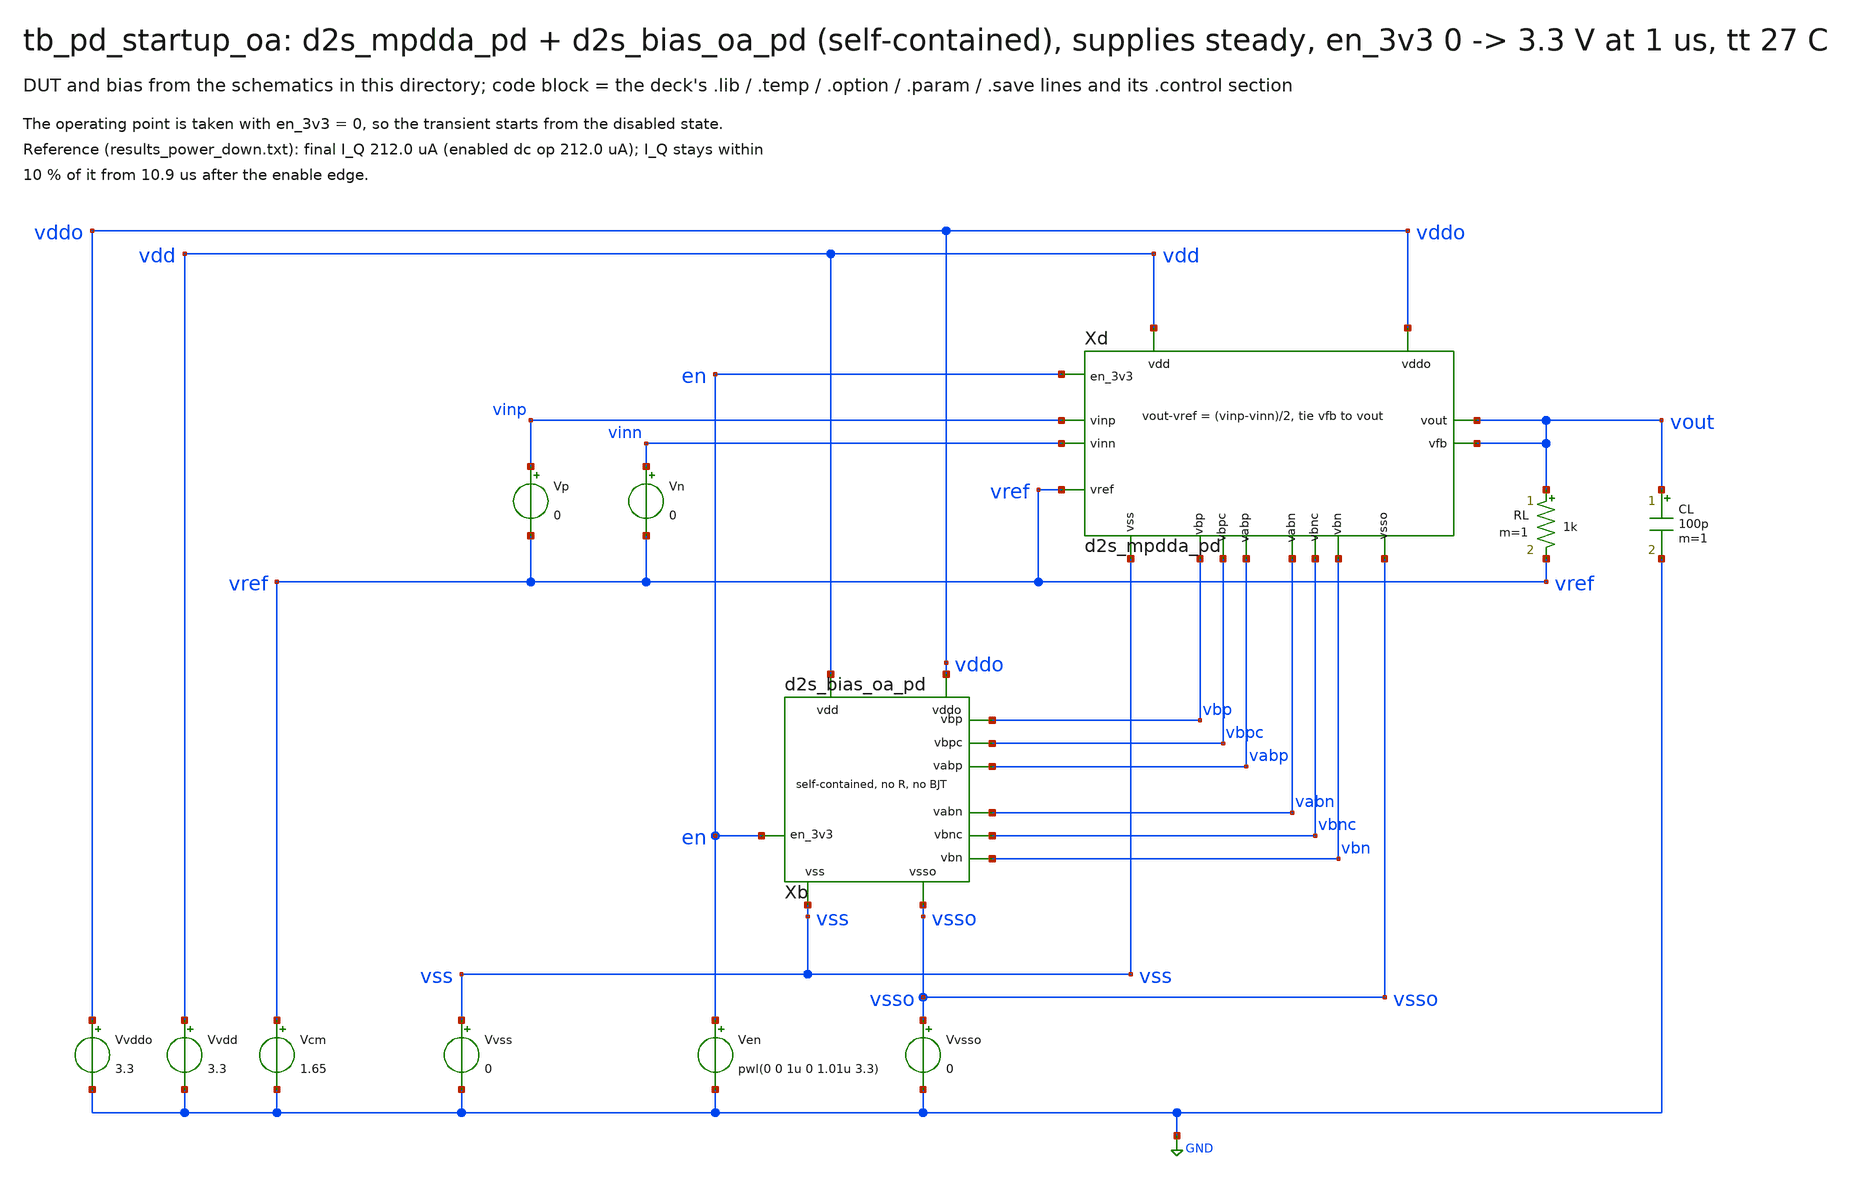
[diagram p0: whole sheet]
** sch_path: sudelbuecher/design_considerations/consolidation/enable_rework_2026-10-25/before/macros/sg13cmos5l_IOPadDiff2Single/testbenches/xschem/tb_pd_startup_oa.sch
**.subckt tb_pd_startup_oa
Vvdd vdd GND 3.3
Vvss vss GND 0
Vvddo vddo GND 3.3
Vvsso vsso GND 0
Ven en GND pwl(0 0 1u 0 1.01u 3.3)
Vcm vref GND 1.65
Xb vdd vss vddo vsso vbp vbn vbpc vbnc vabp vabn en d2s_bias_oa_pd
Xd vdd vss vddo vsso vinp vinn vref vout vout vbp vbn vbpc vbnc vabp vabn en d2s_mpdda_pd
Vp vinp vref 0
Vn vinn vref 0
RL vout vref 1k m=1
CL vout GND 100p m=1
**** begin user architecture code

.lib cornerMOShv.lib mos_tt
.lib cornerRES.lib res_typ
.lib cornerCAP.lib cap_typ
.temp 27
.option method=gear
.save v(vout) v(en) @n.xd.xop.nsg13_hv_pmos[ids] v(xb.xc.vbr) v(xb.xc.ks)
.control
tran 20n 2m
let iq = abs(@n.xd.xop.nsg13_hv_pmos[ids])
meas tran iqf find iq at=2m
let hi = 1.1*iqf
let lo = 0.9*iqf
meas tran t1 when iq=hi cross=last
meas tran t2 when iq=lo cross=last
print iqf t1 t2
if $?batchmode = 0
  plot iq
  plot v(vout) v(xb.xc.vbr) v(xb.xc.ks) xlimit 0 50u
end
.endc

**** end user architecture code
**.ends
.GLOBAL GND
.end
